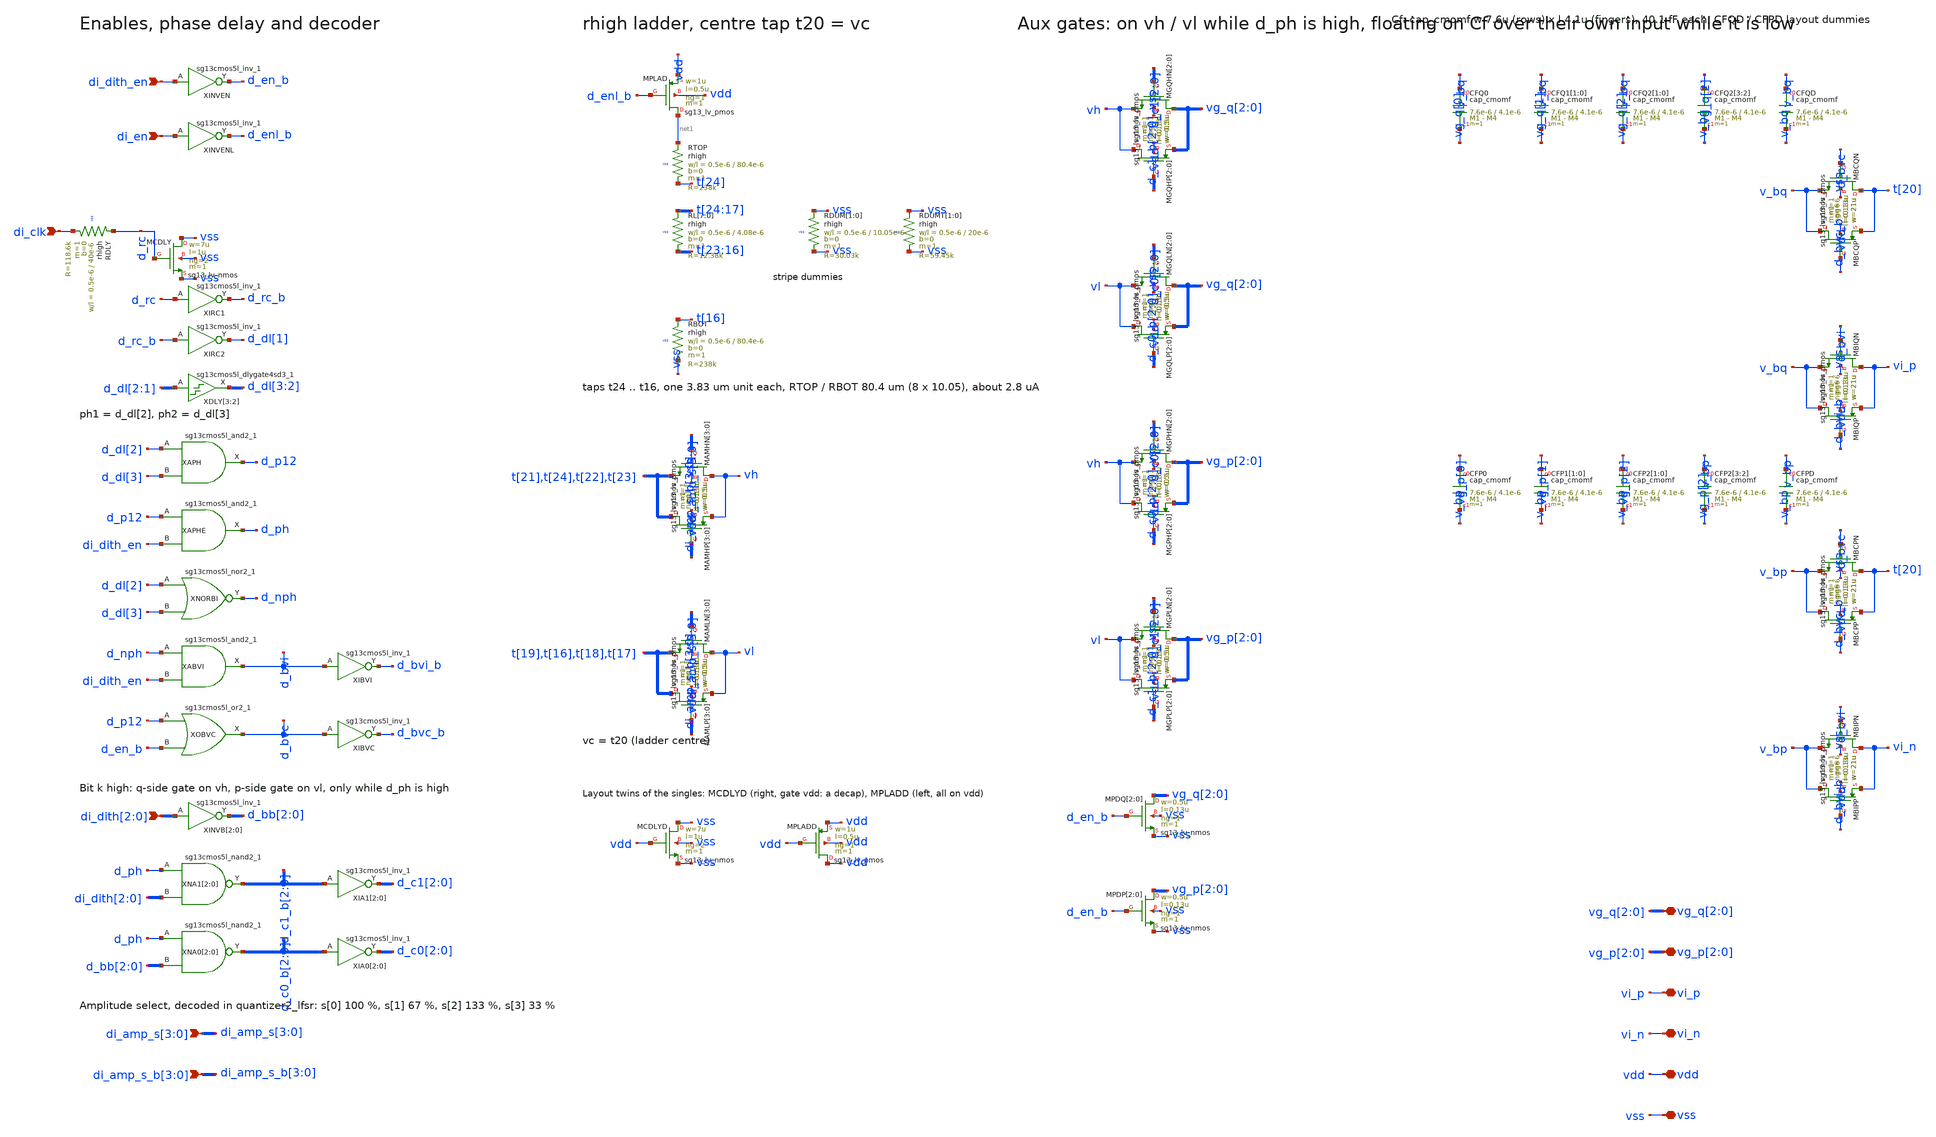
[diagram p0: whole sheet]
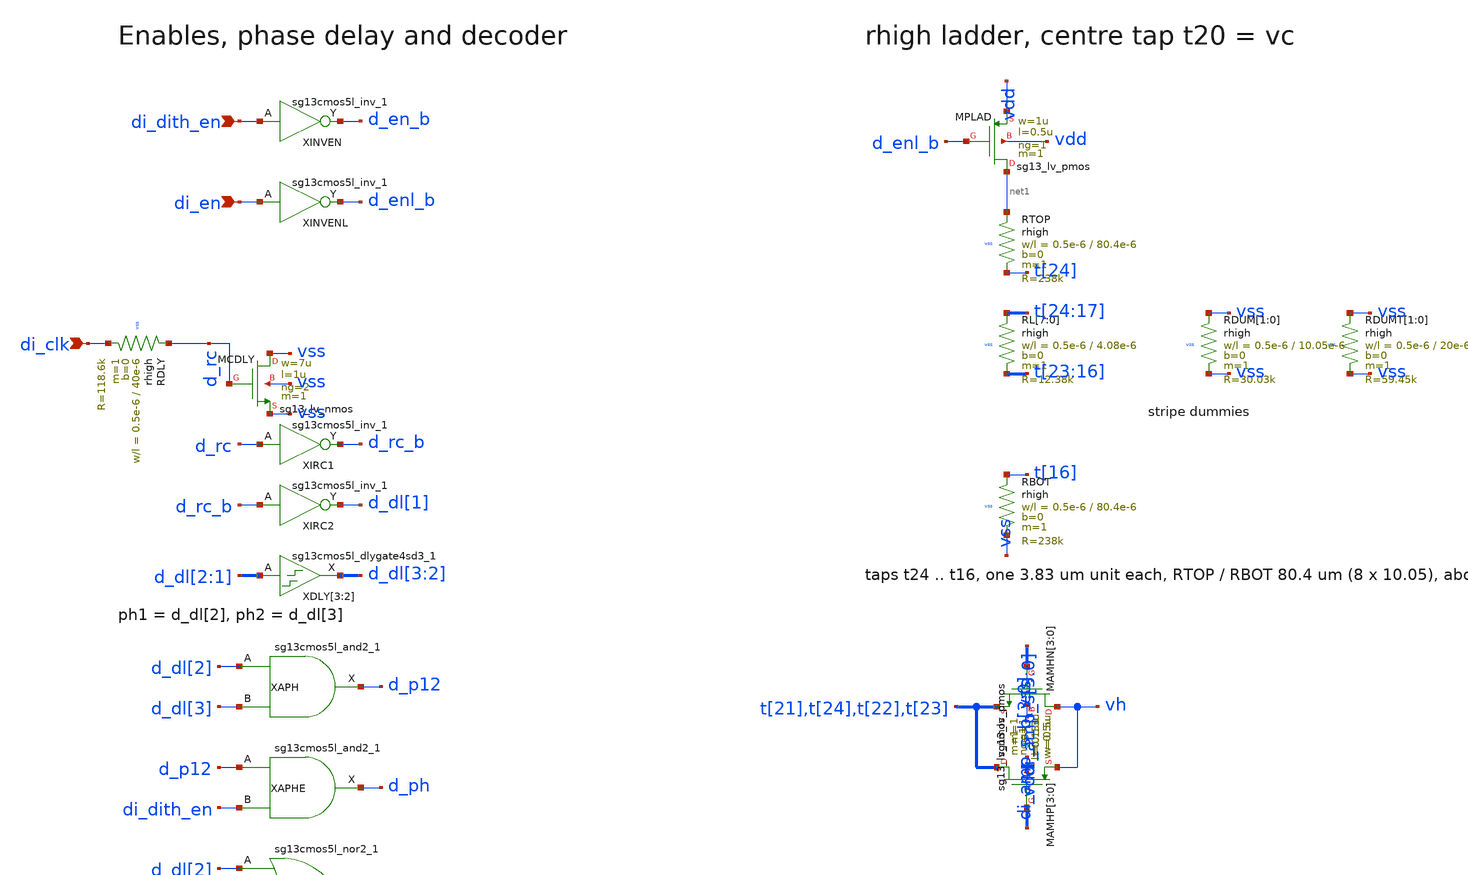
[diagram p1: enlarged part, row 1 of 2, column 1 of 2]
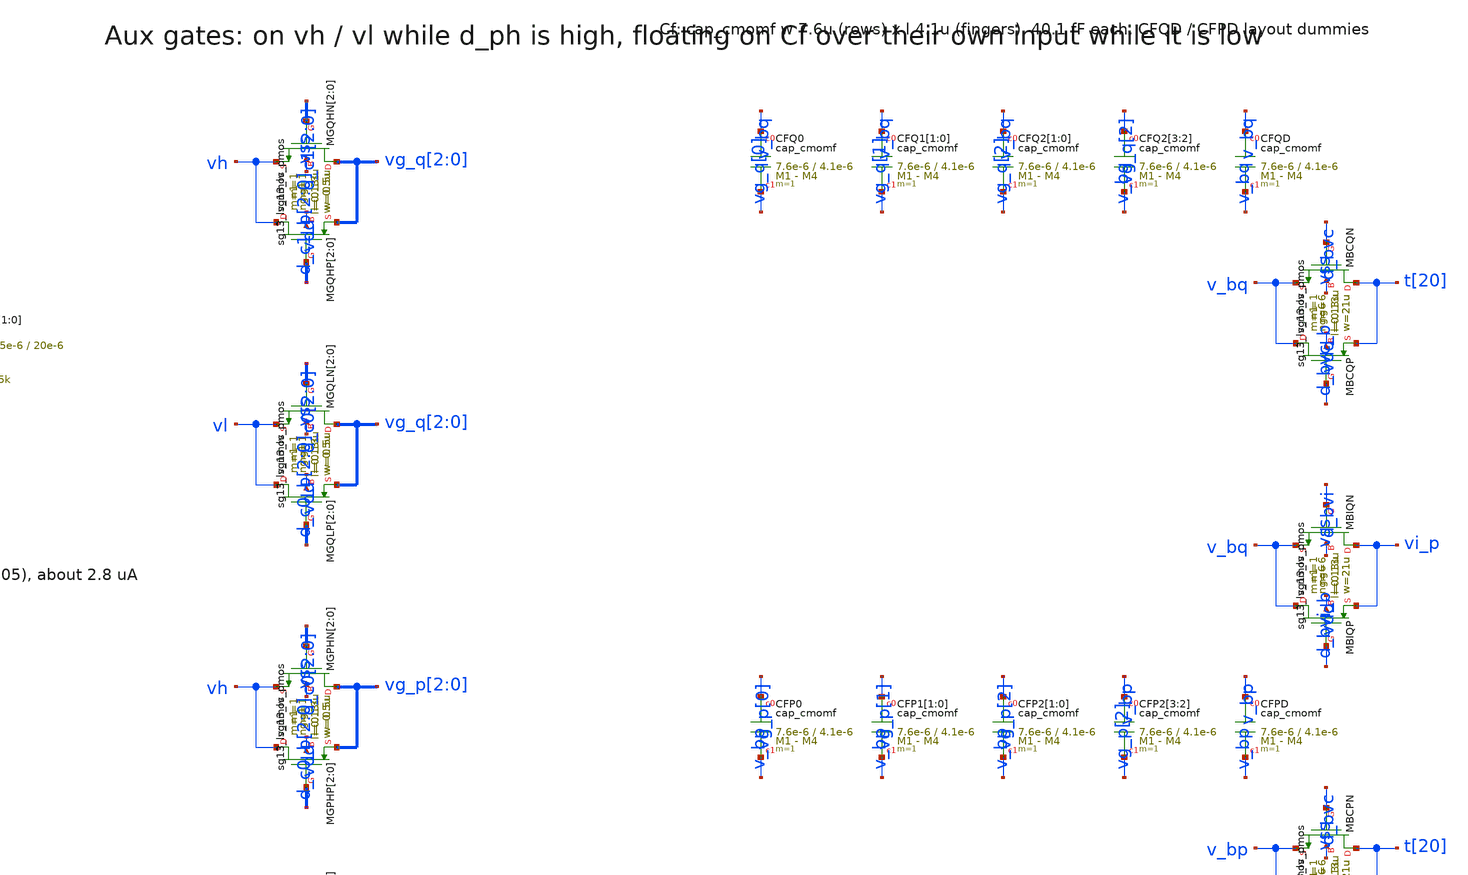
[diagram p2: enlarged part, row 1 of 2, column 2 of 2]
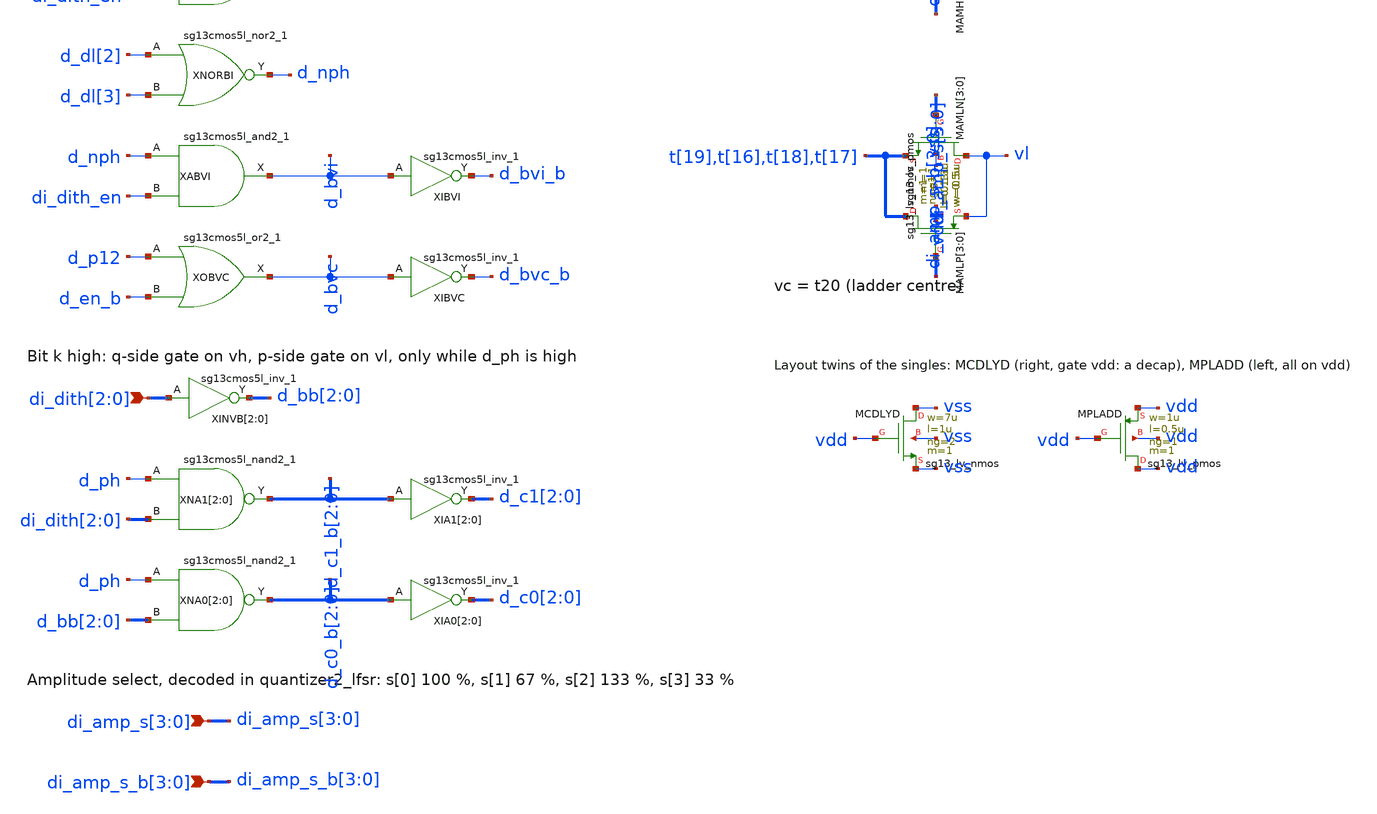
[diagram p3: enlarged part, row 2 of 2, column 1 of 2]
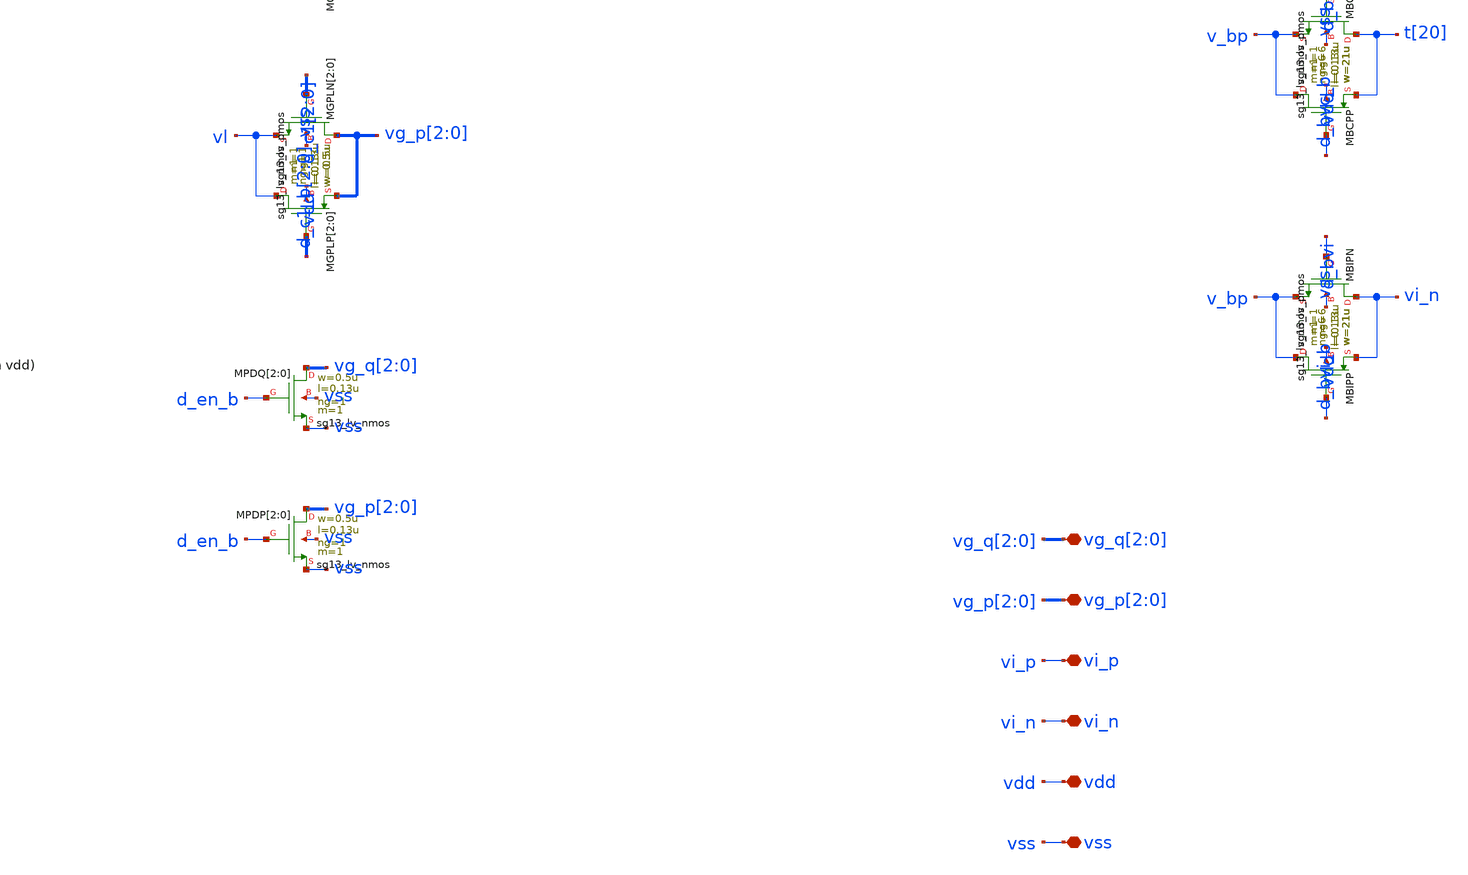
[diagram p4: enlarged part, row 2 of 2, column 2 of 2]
** sch_path: ip/dsm2_core/schematic/quantizer2_dith.sch
* (c) 2026 Michael Koefinger
**.subckt quantizer2_dith di_dith_en di_en di_clk di_dith[2],di_dith[1],di_dith[0]
*+ di_amp_s[3],di_amp_s[2],di_amp_s[1],di_amp_s[0] di_amp_s_b[3],di_amp_s_b[2],di_amp_s_b[1],di_amp_s_b[0] vg_q[2],vg_q[1],vg_q[0]
*+ vg_p[2],vg_p[1],vg_p[0] vi_p vi_n vdd vss
*.ipin di_dith_en
*.ipin di_en
*.ipin di_clk
*.ipin di_dith[2],di_dith[1],di_dith[0]
*.ipin di_amp_s[3],di_amp_s[2],di_amp_s[1],di_amp_s[0]
*.ipin di_amp_s_b[3],di_amp_s_b[2],di_amp_s_b[1],di_amp_s_b[0]
*.iopin vg_q[2],vg_q[1],vg_q[0]
*.iopin vg_p[2],vg_p[1],vg_p[0]
*.iopin vi_p
*.iopin vi_n
*.iopin vdd
*.iopin vss
XINVEN d_en_b di_dith_en vdd vss sg13cmos5l_inv_1
XINVENL d_enl_b di_en vdd vss sg13cmos5l_inv_1
XRDLY d_rc di_clk vss rhigh w=0.5e-6 l=40e-6 m=1 b=0 mm_ok=1
XMCDLY vss d_rc vss vss sg13_lv_nmos w=7u l=1u ng=2 m=1 mm_ok=1
XIRC1 d_rc_b d_rc vdd vss sg13cmos5l_inv_1
XIRC2 d_dl[1] d_rc_b vdd vss sg13cmos5l_inv_1
XDLY[3] d_dl[3] d_dl[2] vdd vss sg13cmos5l_dlygate4sd3_1
XDLY[2] d_dl[2] d_dl[1] vdd vss sg13cmos5l_dlygate4sd3_1
XAPH d_p12 d_dl[2] d_dl[3] vdd vss sg13cmos5l_and2_1
XAPHE d_ph d_p12 di_dith_en vdd vss sg13cmos5l_and2_1
XNORBI d_nph d_dl[2] d_dl[3] vdd vss sg13cmos5l_nor2_1
XABVI d_bvi d_nph di_dith_en vdd vss sg13cmos5l_and2_1
XIBVI d_bvi_b d_bvi vdd vss sg13cmos5l_inv_1
XOBVC d_bvc d_p12 d_en_b vdd vss sg13cmos5l_or2_1
XIBVC d_bvc_b d_bvc vdd vss sg13cmos5l_inv_1
XINVB[2] d_bb[2] di_dith[2] vdd vss sg13cmos5l_inv_1
XINVB[1] d_bb[1] di_dith[1] vdd vss sg13cmos5l_inv_1
XINVB[0] d_bb[0] di_dith[0] vdd vss sg13cmos5l_inv_1
XNA1[2] d_c1_b[2] d_ph di_dith[2] vdd vss sg13cmos5l_nand2_1
XNA1[1] d_c1_b[1] d_ph di_dith[1] vdd vss sg13cmos5l_nand2_1
XNA1[0] d_c1_b[0] d_ph di_dith[0] vdd vss sg13cmos5l_nand2_1
XIA1[2] d_c1[2] d_c1_b[2] vdd vss sg13cmos5l_inv_1
XIA1[1] d_c1[1] d_c1_b[1] vdd vss sg13cmos5l_inv_1
XIA1[0] d_c1[0] d_c1_b[0] vdd vss sg13cmos5l_inv_1
XNA0[2] d_c0_b[2] d_ph d_bb[2] vdd vss sg13cmos5l_nand2_1
XNA0[1] d_c0_b[1] d_ph d_bb[1] vdd vss sg13cmos5l_nand2_1
XNA0[0] d_c0_b[0] d_ph d_bb[0] vdd vss sg13cmos5l_nand2_1
XIA0[2] d_c0[2] d_c0_b[2] vdd vss sg13cmos5l_inv_1
XIA0[1] d_c0[1] d_c0_b[1] vdd vss sg13cmos5l_inv_1
XIA0[0] d_c0[0] d_c0_b[0] vdd vss sg13cmos5l_inv_1
XMPLAD net1 d_enl_b vdd vdd sg13_lv_pmos w=1u l=0.5u ng=1 m=1 mm_ok=1
XRTOP net1 t[24] vss rhigh w=0.5e-6 l=80.4e-6 m=1 b=0 mm_ok=1
XRL[7] t[24] t[23] vss rhigh w=0.5e-6 l=4.08e-6 m=1 b=0 mm_ok=1
XRL[6] t[23] t[22] vss rhigh w=0.5e-6 l=4.08e-6 m=1 b=0 mm_ok=1
XRL[5] t[22] t[21] vss rhigh w=0.5e-6 l=4.08e-6 m=1 b=0 mm_ok=1
XRL[4] t[21] t[20] vss rhigh w=0.5e-6 l=4.08e-6 m=1 b=0 mm_ok=1
XRL[3] t[20] t[19] vss rhigh w=0.5e-6 l=4.08e-6 m=1 b=0 mm_ok=1
XRL[2] t[19] t[18] vss rhigh w=0.5e-6 l=4.08e-6 m=1 b=0 mm_ok=1
XRL[1] t[18] t[17] vss rhigh w=0.5e-6 l=4.08e-6 m=1 b=0 mm_ok=1
XRL[0] t[17] t[16] vss rhigh w=0.5e-6 l=4.08e-6 m=1 b=0 mm_ok=1
XRBOT t[16] vss vss rhigh w=0.5e-6 l=80.4e-6 m=1 b=0 mm_ok=1
XMCDLYD vss vdd vss vss sg13_lv_nmos w=7u l=1u ng=2 m=1 mm_ok=1
XMPLADD vdd vdd vdd vdd sg13_lv_pmos w=1u l=0.5u ng=1 m=1 mm_ok=1
XRDUM[1] vss vss vss rhigh w=0.5e-6 l=10.05e-6 m=1 b=0 mm_ok=1
XRDUM[0] vss vss vss rhigh w=0.5e-6 l=10.05e-6 m=1 b=0 mm_ok=1
XRDUMT[1] vss vss vss rhigh w=0.5e-6 l=20e-6 m=1 b=0 mm_ok=1
XRDUMT[0] vss vss vss rhigh w=0.5e-6 l=20e-6 m=1 b=0 mm_ok=1
XMAMHN[3] vh di_amp_s[3] t[21] vss sg13_lv_nmos w=0.5u l=0.13u ng=1 m=1 mm_ok=1
XMAMHN[2] vh di_amp_s[2] t[24] vss sg13_lv_nmos w=0.5u l=0.13u ng=1 m=1 mm_ok=1
XMAMHN[1] vh di_amp_s[1] t[22] vss sg13_lv_nmos w=0.5u l=0.13u ng=1 m=1 mm_ok=1
XMAMHN[0] vh di_amp_s[0] t[23] vss sg13_lv_nmos w=0.5u l=0.13u ng=1 m=1 mm_ok=1
XMAMHP[3] t[21] di_amp_s_b[3] vh vdd sg13_lv_pmos w=0.5u l=0.13u ng=1 m=1 mm_ok=1
XMAMHP[2] t[24] di_amp_s_b[2] vh vdd sg13_lv_pmos w=0.5u l=0.13u ng=1 m=1 mm_ok=1
XMAMHP[1] t[22] di_amp_s_b[1] vh vdd sg13_lv_pmos w=0.5u l=0.13u ng=1 m=1 mm_ok=1
XMAMHP[0] t[23] di_amp_s_b[0] vh vdd sg13_lv_pmos w=0.5u l=0.13u ng=1 m=1 mm_ok=1
XMAMLN[3] vl di_amp_s[3] t[19] vss sg13_lv_nmos w=0.5u l=0.13u ng=1 m=1 mm_ok=1
XMAMLN[2] vl di_amp_s[2] t[16] vss sg13_lv_nmos w=0.5u l=0.13u ng=1 m=1 mm_ok=1
XMAMLN[1] vl di_amp_s[1] t[18] vss sg13_lv_nmos w=0.5u l=0.13u ng=1 m=1 mm_ok=1
XMAMLN[0] vl di_amp_s[0] t[17] vss sg13_lv_nmos w=0.5u l=0.13u ng=1 m=1 mm_ok=1
XMAMLP[3] t[19] di_amp_s_b[3] vl vdd sg13_lv_pmos w=0.5u l=0.13u ng=1 m=1 mm_ok=1
XMAMLP[2] t[16] di_amp_s_b[2] vl vdd sg13_lv_pmos w=0.5u l=0.13u ng=1 m=1 mm_ok=1
XMAMLP[1] t[18] di_amp_s_b[1] vl vdd sg13_lv_pmos w=0.5u l=0.13u ng=1 m=1 mm_ok=1
XMAMLP[0] t[17] di_amp_s_b[0] vl vdd sg13_lv_pmos w=0.5u l=0.13u ng=1 m=1 mm_ok=1
XMGQHN[2] vg_q[2] d_c1[2] vh vss sg13_lv_nmos w=0.5u l=0.13u ng=1 m=1 mm_ok=1
XMGQHN[1] vg_q[1] d_c1[1] vh vss sg13_lv_nmos w=0.5u l=0.13u ng=1 m=1 mm_ok=1
XMGQHN[0] vg_q[0] d_c1[0] vh vss sg13_lv_nmos w=0.5u l=0.13u ng=1 m=1 mm_ok=1
XMGQHP[2] vh d_c1_b[2] vg_q[2] vdd sg13_lv_pmos w=0.5u l=0.13u ng=1 m=1 mm_ok=1
XMGQHP[1] vh d_c1_b[1] vg_q[1] vdd sg13_lv_pmos w=0.5u l=0.13u ng=1 m=1 mm_ok=1
XMGQHP[0] vh d_c1_b[0] vg_q[0] vdd sg13_lv_pmos w=0.5u l=0.13u ng=1 m=1 mm_ok=1
XMGQLN[2] vg_q[2] d_c0[2] vl vss sg13_lv_nmos w=0.5u l=0.13u ng=1 m=1 mm_ok=1
XMGQLN[1] vg_q[1] d_c0[1] vl vss sg13_lv_nmos w=0.5u l=0.13u ng=1 m=1 mm_ok=1
XMGQLN[0] vg_q[0] d_c0[0] vl vss sg13_lv_nmos w=0.5u l=0.13u ng=1 m=1 mm_ok=1
XMGQLP[2] vl d_c0_b[2] vg_q[2] vdd sg13_lv_pmos w=0.5u l=0.13u ng=1 m=1 mm_ok=1
XMGQLP[1] vl d_c0_b[1] vg_q[1] vdd sg13_lv_pmos w=0.5u l=0.13u ng=1 m=1 mm_ok=1
XMGQLP[0] vl d_c0_b[0] vg_q[0] vdd sg13_lv_pmos w=0.5u l=0.13u ng=1 m=1 mm_ok=1
XMGPHN[2] vg_p[2] d_c0[2] vh vss sg13_lv_nmos w=0.5u l=0.13u ng=1 m=1 mm_ok=1
XMGPHN[1] vg_p[1] d_c0[1] vh vss sg13_lv_nmos w=0.5u l=0.13u ng=1 m=1 mm_ok=1
XMGPHN[0] vg_p[0] d_c0[0] vh vss sg13_lv_nmos w=0.5u l=0.13u ng=1 m=1 mm_ok=1
XMGPHP[2] vh d_c0_b[2] vg_p[2] vdd sg13_lv_pmos w=0.5u l=0.13u ng=1 m=1 mm_ok=1
XMGPHP[1] vh d_c0_b[1] vg_p[1] vdd sg13_lv_pmos w=0.5u l=0.13u ng=1 m=1 mm_ok=1
XMGPHP[0] vh d_c0_b[0] vg_p[0] vdd sg13_lv_pmos w=0.5u l=0.13u ng=1 m=1 mm_ok=1
XMGPLN[2] vg_p[2] d_c1[2] vl vss sg13_lv_nmos w=0.5u l=0.13u ng=1 m=1 mm_ok=1
XMGPLN[1] vg_p[1] d_c1[1] vl vss sg13_lv_nmos w=0.5u l=0.13u ng=1 m=1 mm_ok=1
XMGPLN[0] vg_p[0] d_c1[0] vl vss sg13_lv_nmos w=0.5u l=0.13u ng=1 m=1 mm_ok=1
XMGPLP[2] vl d_c1_b[2] vg_p[2] vdd sg13_lv_pmos w=0.5u l=0.13u ng=1 m=1 mm_ok=1
XMGPLP[1] vl d_c1_b[1] vg_p[1] vdd sg13_lv_pmos w=0.5u l=0.13u ng=1 m=1 mm_ok=1
XMGPLP[0] vl d_c1_b[0] vg_p[0] vdd sg13_lv_pmos w=0.5u l=0.13u ng=1 m=1 mm_ok=1
XMPDQ[2] vg_q[2] d_en_b vss vss sg13_lv_nmos w=0.5u l=0.13u ng=1 m=1 mm_ok=1
XMPDQ[1] vg_q[1] d_en_b vss vss sg13_lv_nmos w=0.5u l=0.13u ng=1 m=1 mm_ok=1
XMPDQ[0] vg_q[0] d_en_b vss vss sg13_lv_nmos w=0.5u l=0.13u ng=1 m=1 mm_ok=1
XMPDP[2] vg_p[2] d_en_b vss vss sg13_lv_nmos w=0.5u l=0.13u ng=1 m=1 mm_ok=1
XMPDP[1] vg_p[1] d_en_b vss vss sg13_lv_nmos w=0.5u l=0.13u ng=1 m=1 mm_ok=1
XMPDP[0] vg_p[0] d_en_b vss vss sg13_lv_nmos w=0.5u l=0.13u ng=1 m=1 mm_ok=1
XCFQ0 v_bq vg_q[0] cap_cmomf w=7.6e-6 l=4.1e-6 mmin=1 mmax=4 subblock=0 m=1 mm_ok=1
XCFQ1[1] v_bq vg_q[1] cap_cmomf w=7.6e-6 l=4.1e-6 mmin=1 mmax=4 subblock=0 m=1 mm_ok=1
XCFQ1[0] v_bq vg_q[1] cap_cmomf w=7.6e-6 l=4.1e-6 mmin=1 mmax=4 subblock=0 m=1 mm_ok=1
XCFQ2[1] v_bq vg_q[2] cap_cmomf w=7.6e-6 l=4.1e-6 mmin=1 mmax=4 subblock=0 m=1 mm_ok=1
XCFQ2[0] v_bq vg_q[2] cap_cmomf w=7.6e-6 l=4.1e-6 mmin=1 mmax=4 subblock=0 m=1 mm_ok=1
XCFQ2[3] vg_q[2] v_bq cap_cmomf w=7.6e-6 l=4.1e-6 mmin=1 mmax=4 subblock=0 m=1 mm_ok=1
XCFQ2[2] vg_q[2] v_bq cap_cmomf w=7.6e-6 l=4.1e-6 mmin=1 mmax=4 subblock=0 m=1 mm_ok=1
XCFQD v_bq v_bq cap_cmomf w=7.6e-6 l=4.1e-6 mmin=1 mmax=4 subblock=0 m=1 mm_ok=1
XMBCQN t[20] d_bvc v_bq vss sg13_lv_nmos w=21u l=0.13u ng=6 m=1 mm_ok=1
XMBCQP v_bq d_bvc_b t[20] vdd sg13_lv_pmos w=21u l=0.13u ng=6 m=1 mm_ok=1
XMBIQN vi_p d_bvi v_bq vss sg13_lv_nmos w=21u l=0.13u ng=6 m=1 mm_ok=1
XMBIQP v_bq d_bvi_b vi_p vdd sg13_lv_pmos w=21u l=0.13u ng=6 m=1 mm_ok=1
XCFP0 vg_p[0] v_bp cap_cmomf w=7.6e-6 l=4.1e-6 mmin=1 mmax=4 subblock=0 m=1 mm_ok=1
XCFP1[1] vg_p[1] v_bp cap_cmomf w=7.6e-6 l=4.1e-6 mmin=1 mmax=4 subblock=0 m=1 mm_ok=1
XCFP1[0] vg_p[1] v_bp cap_cmomf w=7.6e-6 l=4.1e-6 mmin=1 mmax=4 subblock=0 m=1 mm_ok=1
XCFP2[1] vg_p[2] v_bp cap_cmomf w=7.6e-6 l=4.1e-6 mmin=1 mmax=4 subblock=0 m=1 mm_ok=1
XCFP2[0] vg_p[2] v_bp cap_cmomf w=7.6e-6 l=4.1e-6 mmin=1 mmax=4 subblock=0 m=1 mm_ok=1
XCFP2[3] v_bp vg_p[2] cap_cmomf w=7.6e-6 l=4.1e-6 mmin=1 mmax=4 subblock=0 m=1 mm_ok=1
XCFP2[2] v_bp vg_p[2] cap_cmomf w=7.6e-6 l=4.1e-6 mmin=1 mmax=4 subblock=0 m=1 mm_ok=1
XCFPD v_bp v_bp cap_cmomf w=7.6e-6 l=4.1e-6 mmin=1 mmax=4 subblock=0 m=1 mm_ok=1
XMBCPN t[20] d_bvc v_bp vss sg13_lv_nmos w=21u l=0.13u ng=6 m=1 mm_ok=1
XMBCPP v_bp d_bvc_b t[20] vdd sg13_lv_pmos w=21u l=0.13u ng=6 m=1 mm_ok=1
XMBIPN vi_n d_bvi v_bp vss sg13_lv_nmos w=21u l=0.13u ng=6 m=1 mm_ok=1
XMBIPP v_bp d_bvi_b vi_n vdd sg13_lv_pmos w=21u l=0.13u ng=6 m=1 mm_ok=1
**.ends
.end
